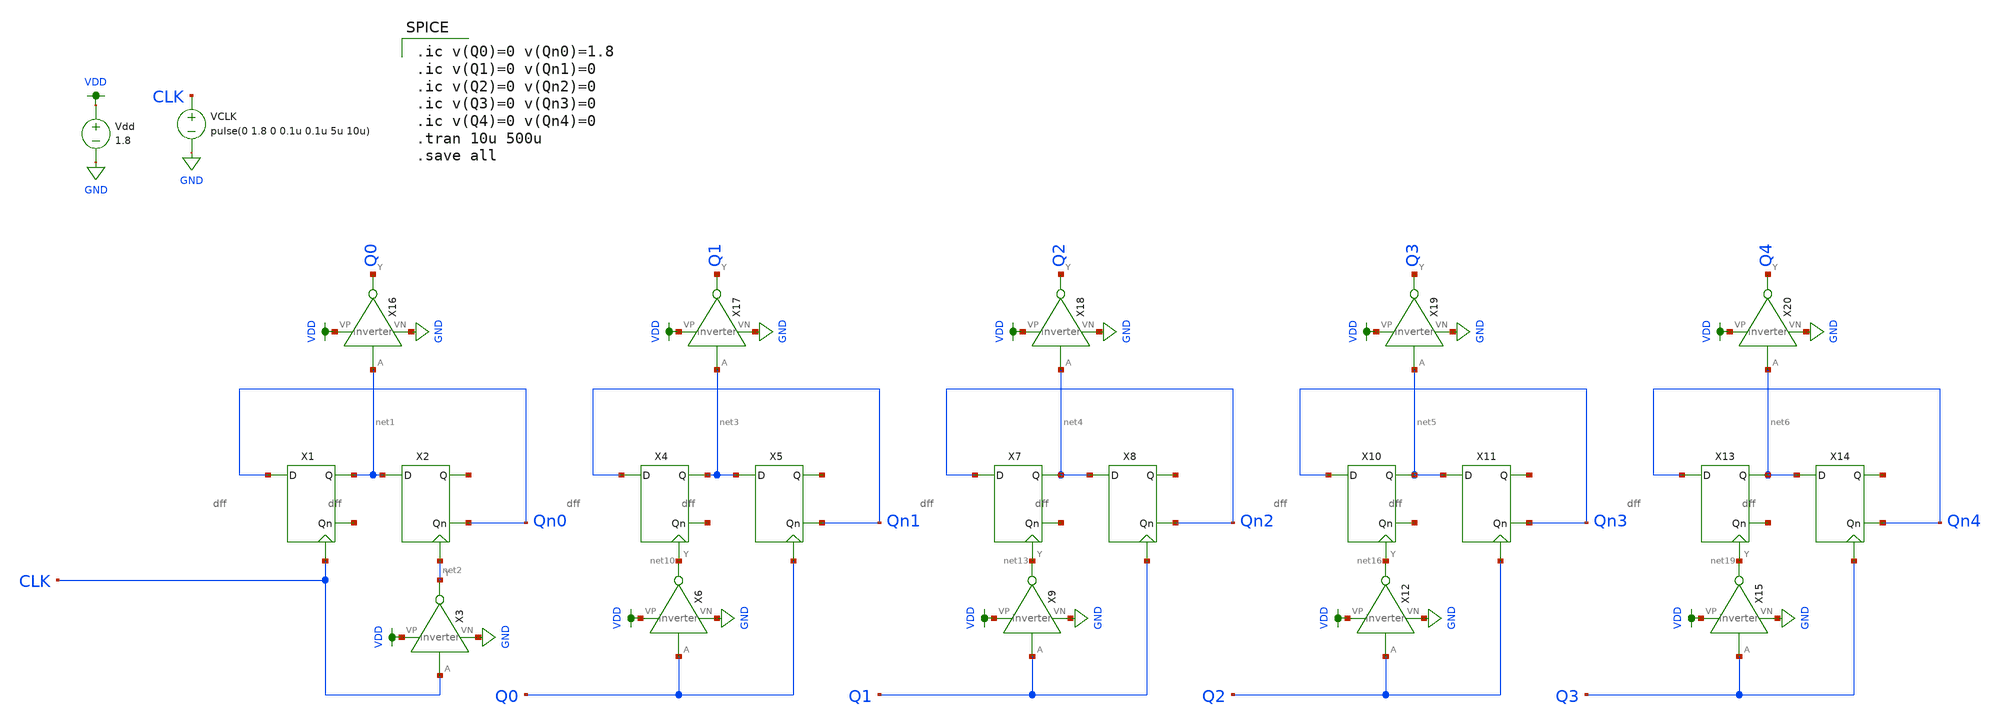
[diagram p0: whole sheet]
** sch_path: schematic/counter_new.sch
**.subckt counter_new
Vdd VDD GND 1.8
VCLK CLK GND pulse(0 1.8 0 0.1u 0.1u 5u 10u)
X1 Qn0 net7 net1 CLK dff
X2 net1 Qn0 net8 net2 dff
X3 CLK net2 VDD GND inverter
X4 Qn1 net9 net3 net10 dff
X5 net3 Qn1 net11 Q0 dff
X6 Q0 net10 VDD GND inverter
X7 Qn2 net12 net4 net13 dff
X8 net4 Qn2 net14 Q1 dff
X10 Qn3 net15 net5 net16 dff
X11 net5 Qn3 net17 Q2 dff
X13 Qn4 net18 net6 net19 dff
X14 net6 Qn4 net20 Q3 dff
X9 Q1 net13 VDD GND inverter
X12 Q2 net16 VDD GND inverter
X15 Q3 net19 VDD GND inverter
X16 net1 Q0 VDD GND inverter
X17 net3 Q1 VDD GND inverter
X18 net4 Q2 VDD GND inverter
X19 net5 Q3 VDD GND inverter
X20 net6 Q4 VDD GND inverter
**** begin user architecture code

.ic v(Q0)=0 v(Qn0)=1.8
.ic v(Q1)=0 v(Qn1)=0
.ic v(Q2)=0 v(Qn2)=0
.ic v(Q3)=0 v(Qn3)=0
.ic v(Q4)=0 v(Qn4)=0
.tran 10u 500u
.save all


.option wnflag=1
.param MC_SWITCH=0.0
.lib ~/skywater/skywater-pdk/libraries/sky130_fd_pr_ngspice/latest/models/sky130.lib.spice tt

**** end user architecture code
**.ends

* expanding   symbol:  /home/madvlsi/Documents/MADVLSI-Final_Project/schematic/dff.sym # of pins=4
** sym_path: schematic/dff.sym
** sch_path: schematic/dff.sch
.subckt dff D Qn Q CLK
*.ipin D
*.iopin CLK
*.opin Qn
*.opin Q
X2 D CLK net1 VDD GND nand2
X3 net3 CLK net2 VDD GND nand2
X4 Q net2 Qn VDD GND nand2
X5 net1 Qn Q VDD GND nand2
X1 D net3 VDD GND inverter
.ends


* expanding   symbol:  /home/madvlsi/Documents/MADVLSI-Final_Project/schematic/inverter.sym # of
*+ pins=4
** sym_path: schematic/inverter.sym
** sch_path: schematic/inverter.sch
.subckt inverter A Y VP VN
*.opin Y
*.ipin A
*.iopin VP
*.iopin VN
XM3 Y A VP VDD sky130_fd_pr__pfet_01v8 L={Lp} W={Wp} nf=1 ad='int((nf+1)/2) * W/nf * 0.29' as='int((nf+2)/2) * W/nf * 0.29'
+ pd='2*int((nf+1)/2) * (W/nf + 0.29)' ps='2*int((nf+2)/2) * (W/nf + 0.29)' nrd='0.29 / W' nrs='0.29 / W'
+ sa=0 sb=0 sd=0 mult=1 m=1
XM4 Y A VP VDD sky130_fd_pr__pfet_01v8 L={Lp} W={Wp} nf=1 ad='int((nf+1)/2) * W/nf * 0.29' as='int((nf+2)/2) * W/nf * 0.29'
+ pd='2*int((nf+1)/2) * (W/nf + 0.29)' ps='2*int((nf+2)/2) * (W/nf + 0.29)' nrd='0.29 / W' nrs='0.29 / W'
+ sa=0 sb=0 sd=0 mult=1 m=1
XM5 Y A VN GND sky130_fd_pr__nfet_01v8 L={Lp} W={Wp} nf=1 ad='int((nf+1)/2) * W/nf * 0.29' as='int((nf+2)/2) * W/nf * 0.29'
+ pd='2*int((nf+1)/2) * (W/nf + 0.29)' ps='2*int((nf+2)/2) * (W/nf + 0.29)' nrd='0.29 / W' nrs='0.29 / W'
+ sa=0 sb=0 sd=0 mult=1 m=1
.ends


* expanding   symbol:  /home/madvlsi/Documents/MADVLSI-Final_Project/schematic/nand2.sym # of pins=5
** sym_path: schematic/nand2.sym
** sch_path: schematic/nand2.sch
.subckt nand2 A B Y VP VN
*.ipin A
*.opin Y
*.ipin B
*.iopin VP
*.iopin VP
*.iopin VN
*.iopin VN
XM1 Y A VP VP sky130_fd_pr__pfet_01v8 L=0.15 W=2 nf=1 ad='int((nf+1)/2) * W/nf * 0.29' as='int((nf+2)/2) * W/nf * 0.29'
+ pd='2*int((nf+1)/2) * (W/nf + 0.29)' ps='2*int((nf+2)/2) * (W/nf + 0.29)' nrd='0.29 / W' nrs='0.29 / W'
+ sa=0 sb=0 sd=0 mult=1 m=1
XM2 VP B Y VP sky130_fd_pr__pfet_01v8 L=0.15 W=2 nf=1 ad='int((nf+1)/2) * W/nf * 0.29' as='int((nf+2)/2) * W/nf * 0.29'
+ pd='2*int((nf+1)/2) * (W/nf + 0.29)' ps='2*int((nf+2)/2) * (W/nf + 0.29)' nrd='0.29 / W' nrs='0.29 / W'
+ sa=0 sb=0 sd=0 mult=1 m=1
XM3 net1 B Y VN sky130_fd_pr__nfet_01v8 L=0.15 W=2 nf=1 ad='int((nf+1)/2) * W/nf * 0.29' as='int((nf+2)/2) * W/nf * 0.29'
+ pd='2*int((nf+1)/2) * (W/nf + 0.29)' ps='2*int((nf+2)/2) * (W/nf + 0.29)' nrd='0.29 / W' nrs='0.29 / W'
+ sa=0 sb=0 sd=0 mult=1 m=1
XM4 net1 A VN VN sky130_fd_pr__nfet_01v8 L=0.15 W=2 nf=1 ad='int((nf+1)/2) * W/nf * 0.29' as='int((nf+2)/2) * W/nf * 0.29'
+ pd='2*int((nf+1)/2) * (W/nf + 0.29)' ps='2*int((nf+2)/2) * (W/nf + 0.29)' nrd='0.29 / W' nrs='0.29 / W'
+ sa=0 sb=0 sd=0 mult=1 m=1
.ends

.GLOBAL GND
.GLOBAL VDD
.end
